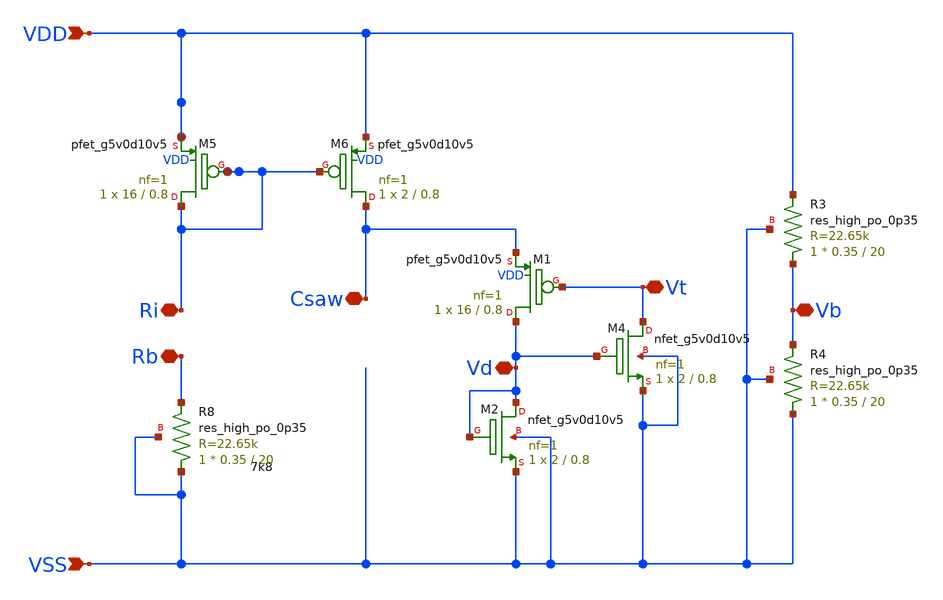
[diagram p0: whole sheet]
** sch_path: xschem/sawgen-fet-sky130.sch
**.subckt sawgen-fet-sky130 VDD VSS Rb Ri Csaw Vt Vb Vd
*.ipin VDD
*.ipin VSS
*.iopin Rb
*.iopin Ri
*.iopin Csaw
*.iopin Vt
*.iopin Vb
*.iopin Vd
XM5 Ri Ri VDD VDD sky130_fd_pr__pfet_g5v0d10v5 L=0.8 W=16 nf=1 ad='int((nf+1)/2) * W/nf * 0.29' as='int((nf+2)/2) * W/nf * 0.29'
+ pd='2*int((nf+1)/2) * (W/nf + 0.29)' ps='2*int((nf+2)/2) * (W/nf + 0.29)' nrd='0.29 / W' nrs='0.29 / W'
+ sa=0 sb=0 sd=0 mult=1 m=1
XM6 Csaw Ri VDD VDD sky130_fd_pr__pfet_g5v0d10v5 L=0.8 W=2 nf=1 ad='int((nf+1)/2) * W/nf * 0.29' as='int((nf+2)/2) * W/nf * 0.29'
+ pd='2*int((nf+1)/2) * (W/nf + 0.29)' ps='2*int((nf+2)/2) * (W/nf + 0.29)' nrd='0.29 / W' nrs='0.29 / W'
+ sa=0 sb=0 sd=0 mult=1 m=1
XR8 VSS Rb VSS sky130_fd_pr__res_high_po_0p35 L=20 mult=1 m=1
XM1 Vd Vt Csaw VDD sky130_fd_pr__pfet_g5v0d10v5 L=0.8 W=16 nf=1 ad='int((nf+1)/2) * W/nf * 0.29' as='int((nf+2)/2) * W/nf * 0.29'
+ pd='2*int((nf+1)/2) * (W/nf + 0.29)' ps='2*int((nf+2)/2) * (W/nf + 0.29)' nrd='0.29 / W' nrs='0.29 / W'
+ sa=0 sb=0 sd=0 mult=1 m=1
XR3 Vb VDD VSS sky130_fd_pr__res_high_po_0p35 L=20 mult=1 m=1
XR4 VSS Vb VSS sky130_fd_pr__res_high_po_0p35 L=20 mult=1 m=1
XM4 Vt Vd VSS VSS sky130_fd_pr__nfet_g5v0d10v5 L=0.8 W=2 nf=1 ad='int((nf+1)/2) * W/nf * 0.29' as='int((nf+2)/2) * W/nf * 0.29'
+ pd='2*int((nf+1)/2) * (W/nf + 0.29)' ps='2*int((nf+2)/2) * (W/nf + 0.29)' nrd='0.29 / W' nrs='0.29 / W'
+ sa=0 sb=0 sd=0 mult=1 m=1
XM2 Vd Vd VSS VSS sky130_fd_pr__nfet_g5v0d10v5 L=0.8 W=2 nf=1 ad='int((nf+1)/2) * W/nf * 0.29' as='int((nf+2)/2) * W/nf * 0.29'
+ pd='2*int((nf+1)/2) * (W/nf + 0.29)' ps='2*int((nf+2)/2) * (W/nf + 0.29)' nrd='0.29 / W' nrs='0.29 / W'
+ sa=0 sb=0 sd=0 mult=1 m=1
**.ends
.end
